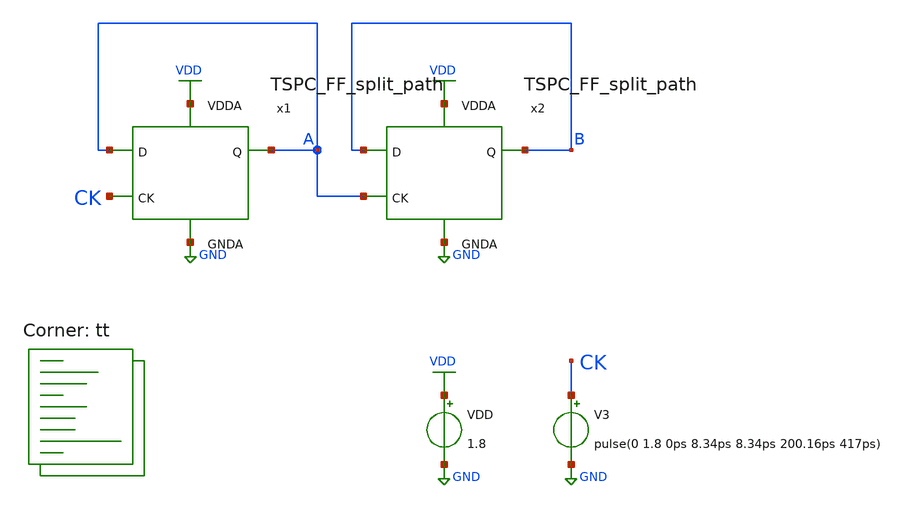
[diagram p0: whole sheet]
** sch_path: projects/pll/divider/xschem_ngspice/tb_TSPC_FF_split_path.sch
**.subckt tb_TSPC_FF_split_path
VDD VDD GND 1.8
V3 CK GND pulse(0 1.8 0ps 8.34ps 8.34ps 200.16ps 417ps)
x2 VDD B B A GND TSPC_FF_split_path
x1 VDD A A CK GND TSPC_FF_split_path
**** begin user architecture code



.include /foss/pdks/sky130A/libs.ref/sky130_fd_sc_hd/spice/sky130_fd_sc_hd.spice

.option method=gear
.option wnflag=1
* .option savecurrents

.save @m.x1.xm1.msky130_fd_pr__pfet_01v8[gm] @m.x1.xm2.msky130_fd_pr__nfet_01v8[gm] @m.x1.xm3.msky130_fd_pr__pfet_01v8[gm] @m.x1.xm4.msky130_fd_pr__nfet_01v8[gm] @m.x1.xm5.msky130_fd_pr__nfet_01v8[gm] @m.x1.xm6.msky130_fd_pr__pfet_01v8[gm] @m.x1.xm7.msky130_fd_pr__pfet_01v8[gm] @m.x1.xm8.msky130_fd_pr__nfet_01v8[gm]
 @m.x2.xm1.msky130_fd_pr__pfet_01v8[gm] @m.x2.xm2.msky130_fd_pr__nfet_01v8[gm]
+ @m.x2.xm3.msky130_fd_pr__pfet_01v8[gm] @m.x2.xm4.msky130_fd_pr__nfet_01v8[gm] @m.x2.xm5.msky130_fd_pr__nfet_01v8[gm]
+ @m.x2.xm6.msky130_fd_pr__pfet_01v8[gm] @m.x2.xm7.msky130_fd_pr__pfet_01v8[gm] @m.x2.xm8.msky130_fd_pr__nfet_01v8[gm]
 @v.x1.vmeas @v.x1.vmeas1 @v.x1.vmeas2 @v.x2.vmeas @v.x2.vmeas1 @v.x2.vmeas2


.control

  * save v(a) v(b) v(ck)
  save all
  *tran 0.1n 1u
  tran 0.2p 5n
  remzerovec
  write tb_TSPC_FF_split_path.raw
  set appendwrite

.endc



.lib $::SKYWATER_MODELS/sky130.lib.spice tt
**** end user architecture code
**.ends

* expanding   symbol:
*+  /foss/designs/my_design/projects/pll/divider/xschem_ngspice/TSPC_FF_split_path.sym # of pins=5
** sym_path: projects/pll/divider/xschem_ngspice/TSPC_FF_split_path.sym
** sch_path: projects/pll/divider/xschem_ngspice/TSPC_FF_split_path.sch
.subckt TSPC_FF_split_path VDDA Q D CK GNDA
*.ipin CK
*.ipin D
*.opin Q
*.ipin VDDA
*.ipin GNDA
XM1 Q B1 VDDA VDDA sky130_fd_pr__pfet_01v8 L=0.15 W=1 nf=1 ad='int((nf+1)/2) * W/nf * 0.29' as='int((nf+2)/2) * W/nf * 0.29'
+ pd='2*int((nf+1)/2) * (W/nf + 0.29)' ps='2*int((nf+2)/2) * (W/nf + 0.29)' nrd='0.29 / W' nrs='0.29 / W'
+ sa=0 sb=0 sd=0 mult=1 m=1
XM4 net1 CK B2 GNDA sky130_fd_pr__nfet_01v8 L=0.15 W=1 nf=1 ad='int((nf+1)/2) * W/nf * 0.29' as='int((nf+2)/2) * W/nf * 0.29'
+ pd='2*int((nf+1)/2) * (W/nf + 0.29)' ps='2*int((nf+2)/2) * (W/nf + 0.29)' nrd='0.29 / W' nrs='0.29 / W'
+ sa=0 sb=0 sd=0 mult=1 m=1
Vmeas Q net3 0
.save i(vmeas)
XM2 net3 B2 GNDA GNDA sky130_fd_pr__nfet_01v8 L=0.15 W=1 nf=1 ad='int((nf+1)/2) * W/nf * 0.29' as='int((nf+2)/2) * W/nf * 0.29'
+ pd='2*int((nf+1)/2) * (W/nf + 0.29)' ps='2*int((nf+2)/2) * (W/nf + 0.29)' nrd='0.29 / W' nrs='0.29 / W'
+ sa=0 sb=0 sd=0 mult=1 m=1
XM3 B1 A1 VDDA VDDA sky130_fd_pr__pfet_01v8 L=0.15 W=1 nf=1 ad='int((nf+1)/2) * W/nf * 0.29' as='int((nf+2)/2) * W/nf * 0.29'
+ pd='2*int((nf+1)/2) * (W/nf + 0.29)' ps='2*int((nf+2)/2) * (W/nf + 0.29)' nrd='0.29 / W' nrs='0.29 / W'
+ sa=0 sb=0 sd=0 mult=1 m=1
XM5 B2 A2 GNDA GNDA sky130_fd_pr__nfet_01v8 L=0.15 W=1 nf=1 ad='int((nf+1)/2) * W/nf * 0.29' as='int((nf+2)/2) * W/nf * 0.29'
+ pd='2*int((nf+1)/2) * (W/nf + 0.29)' ps='2*int((nf+2)/2) * (W/nf + 0.29)' nrd='0.29 / W' nrs='0.29 / W'
+ sa=0 sb=0 sd=0 mult=1 m=1
Vmeas1 B1 net1 0
.save i(vmeas1)
XM6 A1 D VDDA VDDA sky130_fd_pr__pfet_01v8 L=0.15 W=1 nf=1 ad='int((nf+1)/2) * W/nf * 0.29' as='int((nf+2)/2) * W/nf * 0.29'
+ pd='2*int((nf+1)/2) * (W/nf + 0.29)' ps='2*int((nf+2)/2) * (W/nf + 0.29)' nrd='0.29 / W' nrs='0.29 / W'
+ sa=0 sb=0 sd=0 mult=1 m=1
XM8 A2 D GNDA GNDA sky130_fd_pr__nfet_01v8 L=0.15 W=1 nf=1 ad='int((nf+1)/2) * W/nf * 0.29' as='int((nf+2)/2) * W/nf * 0.29'
+ pd='2*int((nf+1)/2) * (W/nf + 0.29)' ps='2*int((nf+2)/2) * (W/nf + 0.29)' nrd='0.29 / W' nrs='0.29 / W'
+ sa=0 sb=0 sd=0 mult=1 m=1
Vmeas2 A1 net2 0
.save i(vmeas2)
XM7 A2 CK net2 VDDA sky130_fd_pr__pfet_01v8 L=0.15 W=1 nf=1 ad='int((nf+1)/2) * W/nf * 0.29' as='int((nf+2)/2) * W/nf * 0.29'
+ pd='2*int((nf+1)/2) * (W/nf + 0.29)' ps='2*int((nf+2)/2) * (W/nf + 0.29)' nrd='0.29 / W' nrs='0.29 / W'
+ sa=0 sb=0 sd=0 mult=1 m=1
.ends

.GLOBAL GND
.GLOBAL VDD
.end
